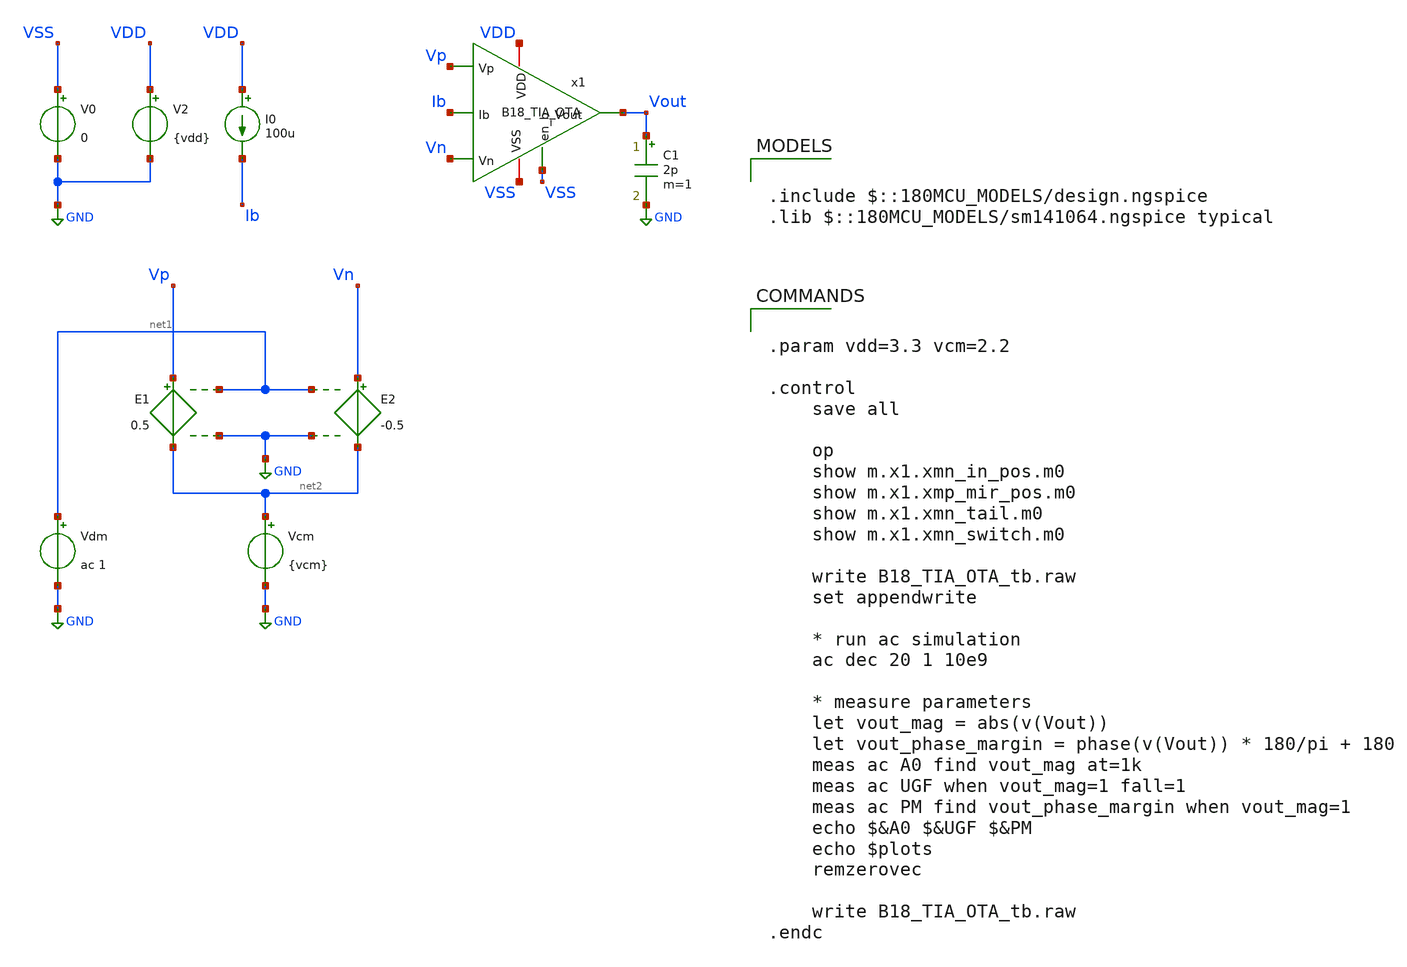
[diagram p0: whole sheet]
** sch_path: Analog/schematics/1_readout/tia/B18_TIA_OTA_tb.sch
**.subckt B18_TIA_OTA_tb
I0 VDD Ib 100u
C1 Vout GND 2p m=1
V0 VSS GND 0
V2 VDD GND {vdd}
E1 Vp net2 net1 GND 0.5
E2 Vn net2 net1 GND -0.5
Vdm net1 GND ac 1
Vcm net2 GND {vcm}
x1 Vp Vn Vout VDD VSS Ib VSS B18_TIA_OTA
**** begin user architecture code


.param vdd=3.3 vcm=2.2

.control
    save all

    op
    show m.x1.xmn_in_pos.m0
    show m.x1.xmp_mir_pos.m0
    show m.x1.xmn_tail.m0
    show m.x1.xmn_switch.m0

    write B18_TIA_OTA_tb.raw
    set appendwrite

    * run ac simulation
    ac dec 20 1 10e9

    * measure parameters
    let vout_mag = abs(v(Vout))
    let vout_phase_margin = phase(v(Vout)) * 180/pi + 180
    meas ac A0 find vout_mag at=1k
    meas ac UGF when vout_mag=1 fall=1
    meas ac PM find vout_phase_margin when vout_mag=1
    echo $&A0 $&UGF $&PM
    echo $plots
    remzerovec

    write B18_TIA_OTA_tb.raw
.endc



.include $::180MCU_MODELS/design.ngspice
.lib $::180MCU_MODELS/sm141064.ngspice typical

**** end user architecture code
**.ends

* expanding   symbol:  Analog/schematics/1_readout/tia/B18_TIA_OTA.sym # of pins=7
** sym_path: Analog/schematics/1_readout/tia/B18_TIA_OTA.sym
** sch_path: Analog/schematics/1_readout/tia/B18_TIA_OTA.sch
.subckt B18_TIA_OTA Vp Vn Vout VDD VSS Ib en_b
*.ipin Vp
*.ipin Vn
*.opin Vout
*.iopin VDD
*.iopin VSS
*.ipin Ib
*.ipin en_b
XMP_MIR_NEG Vout net1 VDD VDD pfet_03v3 L=0.5u W=70u nf=14 ad='int((nf+1)/2) * W/nf * 0.18u' as='int((nf+2)/2) * W/nf * 0.18u'
+ pd='2*int((nf+1)/2) * (W/nf + 0.18u)' ps='2*int((nf+2)/2) * (W/nf + 0.18u)' nrd='0.18u / W' nrs='0.18u / W'
+ sa=0 sb=0 sd=0 m=1
XMP_MIR_POS net1 net1 VDD VDD pfet_03v3 L=0.5u W=70u nf=14 ad='int((nf+1)/2) * W/nf * 0.18u' as='int((nf+2)/2) * W/nf * 0.18u'
+ pd='2*int((nf+1)/2) * (W/nf + 0.18u)' ps='2*int((nf+2)/2) * (W/nf + 0.18u)' nrd='0.18u / W' nrs='0.18u / W'
+ sa=0 sb=0 sd=0 m=1
XMN_IN_POS net1 Vp net2 VSS nfet_03v3 L=0.5u W=20u nf=4 ad='int((nf+1)/2) * W/nf * 0.18u' as='int((nf+2)/2) * W/nf * 0.18u'
+ pd='2*int((nf+1)/2) * (W/nf + 0.18u)' ps='2*int((nf+2)/2) * (W/nf + 0.18u)' nrd='0.18u / W' nrs='0.18u / W'
+ sa=0 sb=0 sd=0 m=1
XMN_IN_NEG Vout Vn net2 VSS nfet_03v3 L=0.5u W=20u nf=4 ad='int((nf+1)/2) * W/nf * 0.18u' as='int((nf+2)/2) * W/nf * 0.18u'
+ pd='2*int((nf+1)/2) * (W/nf + 0.18u)' ps='2*int((nf+2)/2) * (W/nf + 0.18u)' nrd='0.18u / W' nrs='0.18u / W'
+ sa=0 sb=0 sd=0 m=1
XMN_TAIL net2 Ib VSS VSS nfet_03v3 L=0.5u W=40u nf=8 ad='int((nf+1)/2) * W/nf * 0.18u' as='int((nf+2)/2) * W/nf * 0.18u'
+ pd='2*int((nf+1)/2) * (W/nf + 0.18u)' ps='2*int((nf+2)/2) * (W/nf + 0.18u)' nrd='0.18u / W' nrs='0.18u / W'
+ sa=0 sb=0 sd=0 m=1
XMN_TAILMIR Ib Ib VSS VSS nfet_03v3 L=0.5u W=40u nf=8 ad='int((nf+1)/2) * W/nf * 0.18u' as='int((nf+2)/2) * W/nf * 0.18u'
+ pd='2*int((nf+1)/2) * (W/nf + 0.18u)' ps='2*int((nf+2)/2) * (W/nf + 0.18u)' nrd='0.18u / W' nrs='0.18u / W'
+ sa=0 sb=0 sd=0 m=1
XMN_SWITCH Ib en_b VSS VSS nfet_03v3 L=0.5u W=1u nf=1 ad='int((nf+1)/2) * W/nf * 0.18u' as='int((nf+2)/2) * W/nf * 0.18u'
+ pd='2*int((nf+1)/2) * (W/nf + 0.18u)' ps='2*int((nf+2)/2) * (W/nf + 0.18u)' nrd='0.18u / W' nrs='0.18u / W'
+ sa=0 sb=0 sd=0 m=1
**** begin user architecture code


* B18_TIA_OTA

* Original Design Specifications:
  * gm_id for all transistors is 12 V^-1 (moderate inversion)
  * C_L = 2pF
  * GBW = 50MHz
  * L = 0.5um

* Results using pygmid:

*             MN_TAIL  MN_IN   MP_MIR

*  W(um)      38.5     19.25   66.52
*  nf@W=5um   8        4       14
*  Id(uA)     105      52.4    52.4



* The enable signal is a simple NMOS gate pulldown transistor
* placed at the tail current mirror. Assuming a digital signal
* of 3.3V is present, the active-low switch will turn off the
* current mirror


**** end user architecture code
.ends

.GLOBAL GND
.end
